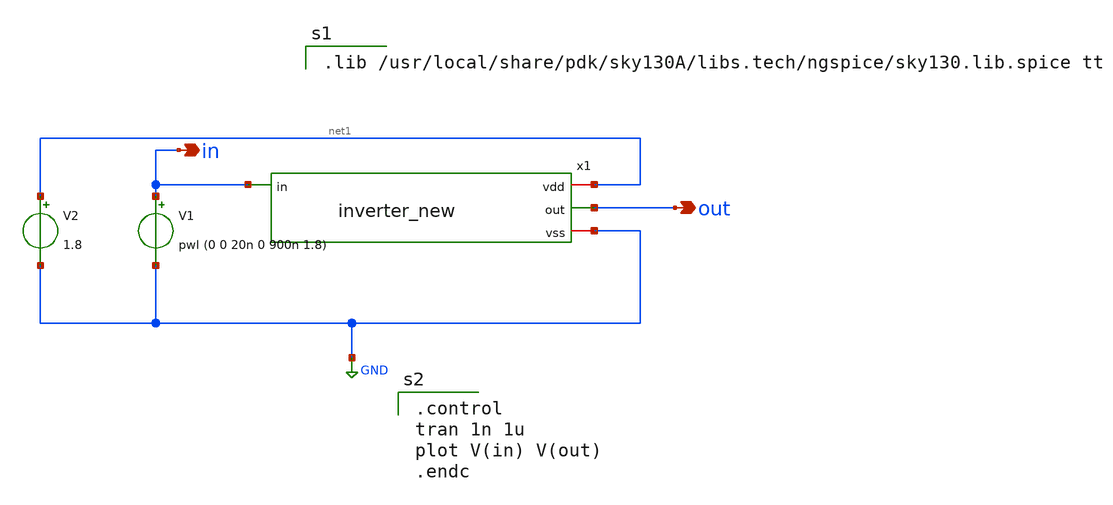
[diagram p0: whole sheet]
** sch_path: inverter_new/xschem/inverter_new_tb.sch
**.subckt inverter_new_tb out in
*.opin out
*.opin in
x1 net1 in out GND inverter_new
V1 in GND pwl (0 0 20n 0 900n 1.8)
V2 net1 GND 1.8
**** begin user architecture code

.lib /usr/local/share/pdk/sky130A/libs.tech/ngspice/sky130.lib.spice tt


.control
tran 1n 1u
plot V(in) V(out)
.endc

**** end user architecture code
**.ends

* expanding   symbol:  inverter_new.sym # of pins=4
** sym_path: inverter_new/xschem/inverter_new.sym
** sch_path: inverter_new/xschem/inverter_new.sch
.subckt inverter_new vdd in out vss
*.ipin in
*.iopin vdd
*.iopin vss
*.opin out
XM2 out in vdd vdd sky130_fd_pr__pfet_01v8 L=0.18 W=3 nf=3 ad='int((nf+1)/2) * W/nf * 0.29' as='int((nf+2)/2) * W/nf * 0.29'
+ pd='2*int((nf+1)/2) * (W/nf + 0.29)' ps='2*int((nf+2)/2) * (W/nf + 0.29)' nrd='0.29 / W' nrs='0.29 / W'
+ sa=0 sb=0 sd=0 mult=1 m=1
XM1 out in vss vss sky130_fd_pr__nfet_01v8 L=0.2 W=4.5 nf=1 ad='int((nf+1)/2) * W/nf * 0.29' as='int((nf+2)/2) * W/nf * 0.29'
+ pd='2*int((nf+1)/2) * (W/nf + 0.29)' ps='2*int((nf+2)/2) * (W/nf + 0.29)' nrd='0.29 / W' nrs='0.29 / W'
+ sa=0 sb=0 sd=0 mult=1 m=1
.ends

.GLOBAL GND
.end
